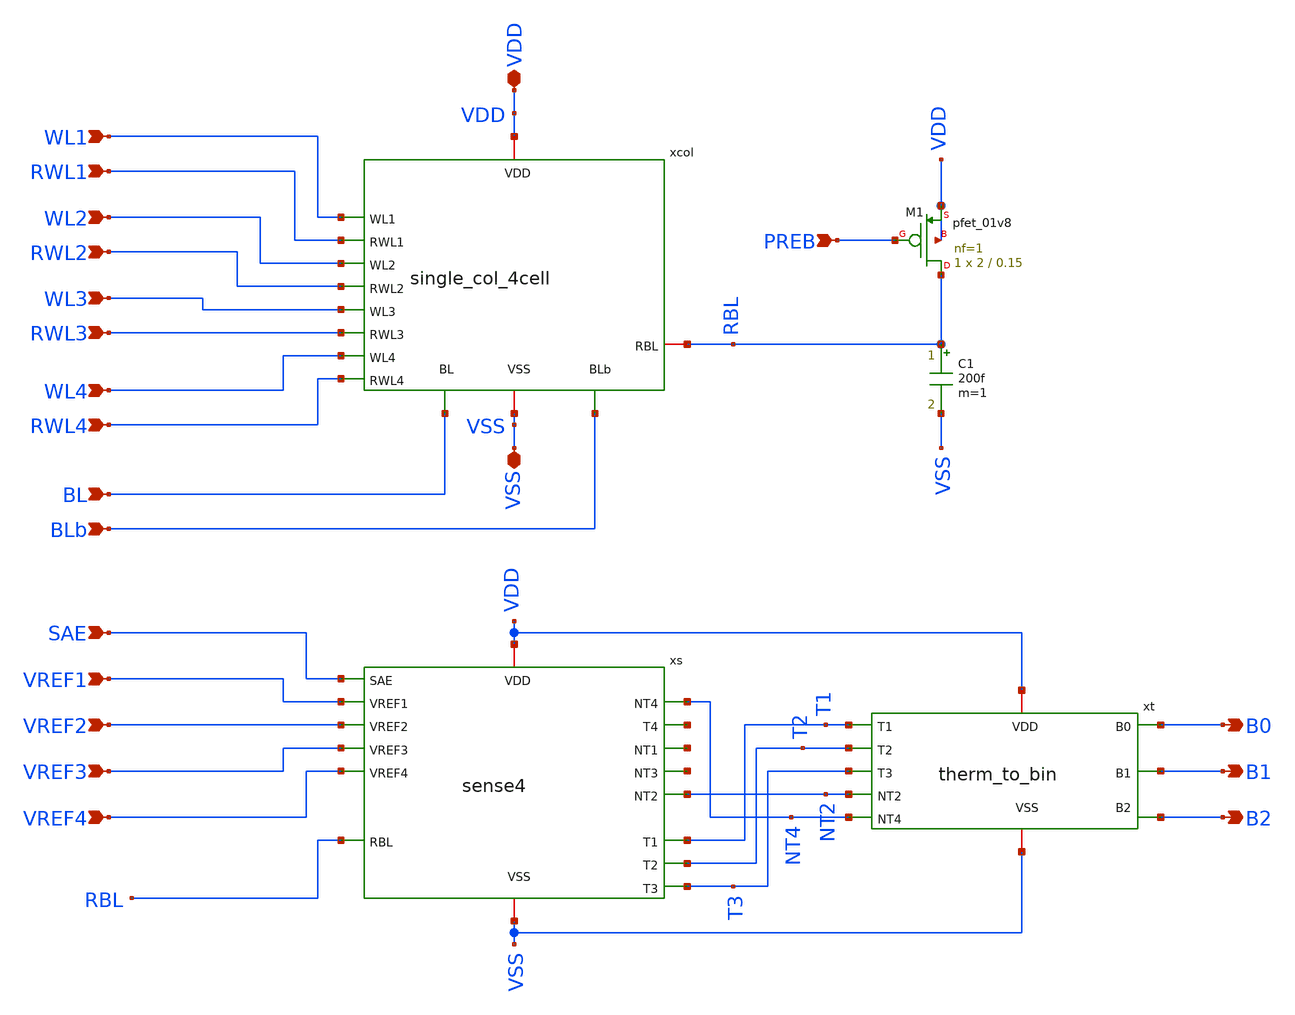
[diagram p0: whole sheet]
** sch_path: schematics/cim_column.sch
**.subckt cim_column VDD VSS WL1 RWL1 WL2 RWL2 WL3 RWL3 WL4 RWL4 BL BLb PREB SAE VREF1 VREF2 VREF3
*+ VREF4 B0 B1 B2
*.iopin VDD
*.iopin VSS
*.ipin WL1
*.ipin RWL1
*.ipin WL2
*.ipin RWL2
*.ipin WL3
*.ipin RWL3
*.ipin WL4
*.ipin RWL4
*.ipin BL
*.ipin BLb
*.ipin PREB
*.ipin SAE
*.ipin VREF1
*.ipin VREF2
*.ipin VREF3
*.ipin VREF4
*.opin B0
*.opin B1
*.opin B2
xcol WL1 VDD BL BLb RBL RWL1 WL2 RWL2 WL3 RWL3 WL4 RWL4 VSS single_col_4cell
XM1 RBL PREB VDD VDD sky130_fd_pr__pfet_01v8 L=0.15 W=2 nf=1 ad='int((1 + 1)/2) * 2 / 1 * 0.29' as='int((1 + 2)/2) * 2 / 1 * 0.29'
+ pd='2*int((1 + 1)/2) * (2 / 1 + 0.29)' ps='2*int((1 + 2)/2) * (2 / 1 + 0.29)' nrd='0.29 / 2 ' nrs='0.29 / 2 '
+ sa=0 sb=0 sd=0 mult=1 m=1
C1 RBL VSS 200f m=1
xs VDD SAE VREF1 VREF3 VREF2 RBL VREF4 NT4 net1 net2 net3 NT2 VSS T1 T2 T3 sense4
xt VDD T3 T1 T2 NT4 NT2 VSS B0 B1 B2 therm_to_bin
**.ends
.end
